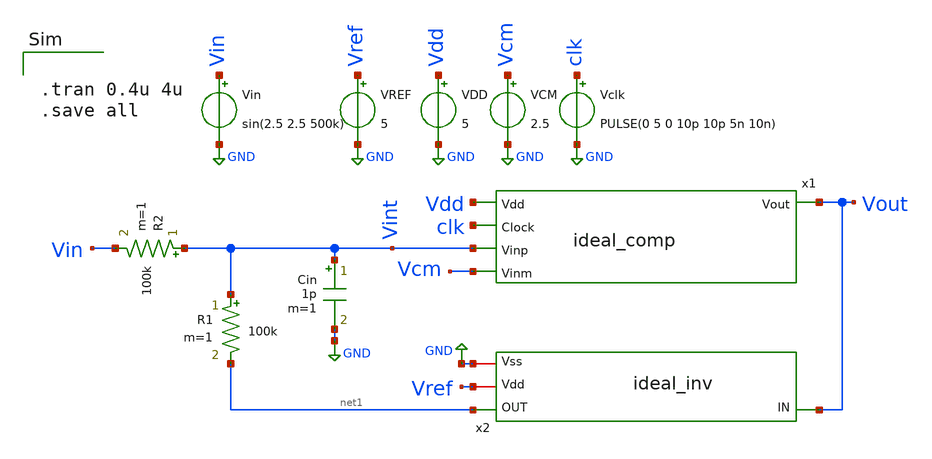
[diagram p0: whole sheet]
** sch_path: ideal_circuit/xschem/ideal_circuit_simple.sch
**.subckt ideal_circuit_simple
VDD Vdd GND 5
VCM Vcm GND 2.5
Vin Vin GND sin(2.5 2.5 500k)
Cin Vint GND 1p m=1
Vclk clk GND PULSE(0 5 0 10p 10p 5n 10n)
R1 Vint net1 100k m=1
R2 Vint Vin 100k m=1
VREF Vref GND 5
x2 net1 Vref Vout GND ideal_inv
x1 Vout Vdd clk Vint Vcm ideal_comp
**** begin user architecture code


.tran 0.4u 4u
.save all


**** end user architecture code
**.ends
.GLOBAL GND
.end
